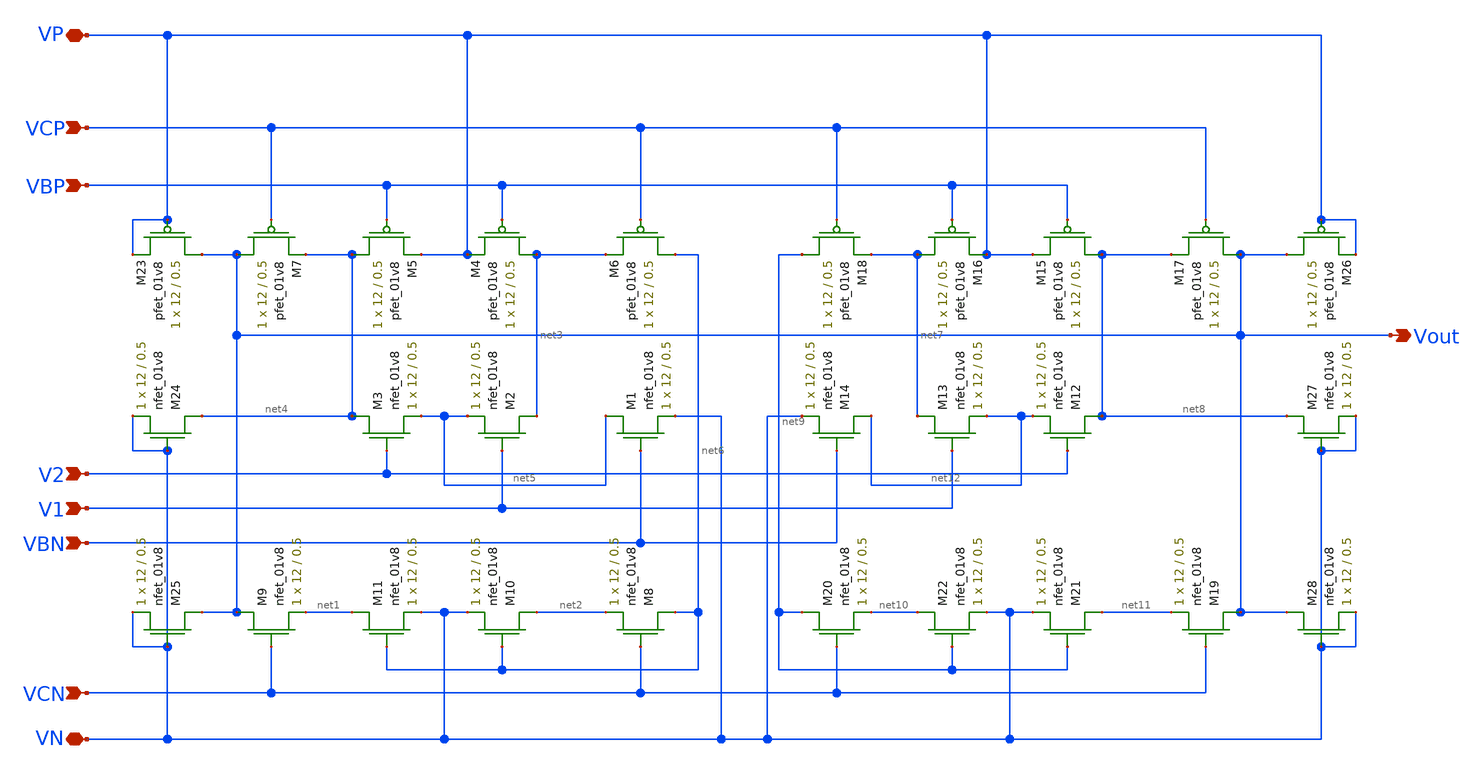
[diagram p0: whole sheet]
** sch_path: mp3/diff_amp/diff_amp_LDS_v3.sch
**.subckt diff_amp_LDS_v3 V1 V2 VN VBN VBP VP VCP VCN Vout
*.ipin V1
*.ipin V2
*.iopin VN
*.ipin VBN
*.ipin VBP
*.iopin VP
*.ipin VCP
*.ipin VCN
*.opin Vout
XM1 net5 VBN VN VN sky130_fd_pr__nfet_01v8 L=0.5 W=12 nf=1 ad='int((nf+1)/2) * W/nf * 0.29' as='int((nf+2)/2) * W/nf * 0.29'
+ pd='2*int((nf+1)/2) * (W/nf + 0.29)' ps='2*int((nf+2)/2) * (W/nf + 0.29)' nrd='0.29 / W' nrs='0.29 / W'
+ sa=0 sb=0 sd=0 mult=1 m=1
XM2 net3 V1 net5 VN sky130_fd_pr__nfet_01v8 L=0.5 W=12 nf=1 ad='int((nf+1)/2) * W/nf * 0.29' as='int((nf+2)/2) * W/nf * 0.29'
+ pd='2*int((nf+1)/2) * (W/nf + 0.29)' ps='2*int((nf+2)/2) * (W/nf + 0.29)' nrd='0.29 / W' nrs='0.29 / W'
+ sa=0 sb=0 sd=0 mult=1 m=1
XM3 net4 V2 net5 VN sky130_fd_pr__nfet_01v8 L=0.5 W=12 nf=1 ad='int((nf+1)/2) * W/nf * 0.29' as='int((nf+2)/2) * W/nf * 0.29'
+ pd='2*int((nf+1)/2) * (W/nf + 0.29)' ps='2*int((nf+2)/2) * (W/nf + 0.29)' nrd='0.29 / W' nrs='0.29 / W'
+ sa=0 sb=0 sd=0 mult=1 m=1
XM4 net3 VBP VP VP sky130_fd_pr__pfet_01v8 L=0.5 W=12 nf=1 ad='int((nf+1)/2) * W/nf * 0.29' as='int((nf+2)/2) * W/nf * 0.29'
+ pd='2*int((nf+1)/2) * (W/nf + 0.29)' ps='2*int((nf+2)/2) * (W/nf + 0.29)' nrd='0.29 / W' nrs='0.29 / W'
+ sa=0 sb=0 sd=0 mult=1 m=1
XM5 net4 VBP VP VP sky130_fd_pr__pfet_01v8 L=0.5 W=12 nf=1 ad='int((nf+1)/2) * W/nf * 0.29' as='int((nf+2)/2) * W/nf * 0.29'
+ pd='2*int((nf+1)/2) * (W/nf + 0.29)' ps='2*int((nf+2)/2) * (W/nf + 0.29)' nrd='0.29 / W' nrs='0.29 / W'
+ sa=0 sb=0 sd=0 mult=1 m=1
XM6 net6 VCP net3 VP sky130_fd_pr__pfet_01v8 L=0.5 W=12 nf=1 ad='int((nf+1)/2) * W/nf * 0.29' as='int((nf+2)/2) * W/nf * 0.29'
+ pd='2*int((nf+1)/2) * (W/nf + 0.29)' ps='2*int((nf+2)/2) * (W/nf + 0.29)' nrd='0.29 / W' nrs='0.29 / W'
+ sa=0 sb=0 sd=0 mult=1 m=1
XM7 Vout VCP net4 VP sky130_fd_pr__pfet_01v8 L=0.5 W=12 nf=1 ad='int((nf+1)/2) * W/nf * 0.29' as='int((nf+2)/2) * W/nf * 0.29'
+ pd='2*int((nf+1)/2) * (W/nf + 0.29)' ps='2*int((nf+2)/2) * (W/nf + 0.29)' nrd='0.29 / W' nrs='0.29 / W'
+ sa=0 sb=0 sd=0 mult=1 m=1
XM8 net6 VCN net2 VN sky130_fd_pr__nfet_01v8 L=0.5 W=12 nf=1 ad='int((nf+1)/2) * W/nf * 0.29' as='int((nf+2)/2) * W/nf * 0.29'
+ pd='2*int((nf+1)/2) * (W/nf + 0.29)' ps='2*int((nf+2)/2) * (W/nf + 0.29)' nrd='0.29 / W' nrs='0.29 / W'
+ sa=0 sb=0 sd=0 mult=1 m=1
XM9 Vout VCN net1 VN sky130_fd_pr__nfet_01v8 L=0.5 W=12 nf=1 ad='int((nf+1)/2) * W/nf * 0.29' as='int((nf+2)/2) * W/nf * 0.29'
+ pd='2*int((nf+1)/2) * (W/nf + 0.29)' ps='2*int((nf+2)/2) * (W/nf + 0.29)' nrd='0.29 / W' nrs='0.29 / W'
+ sa=0 sb=0 sd=0 mult=1 m=1
XM10 net2 net6 VN VN sky130_fd_pr__nfet_01v8 L=0.5 W=12 nf=1 ad='int((nf+1)/2) * W/nf * 0.29' as='int((nf+2)/2) * W/nf * 0.29'
+ pd='2*int((nf+1)/2) * (W/nf + 0.29)' ps='2*int((nf+2)/2) * (W/nf + 0.29)' nrd='0.29 / W' nrs='0.29 / W'
+ sa=0 sb=0 sd=0 mult=1 m=1
XM11 net1 net6 VN VN sky130_fd_pr__nfet_01v8 L=0.5 W=12 nf=1 ad='int((nf+1)/2) * W/nf * 0.29' as='int((nf+2)/2) * W/nf * 0.29'
+ pd='2*int((nf+1)/2) * (W/nf + 0.29)' ps='2*int((nf+2)/2) * (W/nf + 0.29)' nrd='0.29 / W' nrs='0.29 / W'
+ sa=0 sb=0 sd=0 mult=1 m=1
XM12 net8 V2 net12 VN sky130_fd_pr__nfet_01v8 L=0.5 W=12 nf=1 ad='int((nf+1)/2) * W/nf * 0.29' as='int((nf+2)/2) * W/nf * 0.29'
+ pd='2*int((nf+1)/2) * (W/nf + 0.29)' ps='2*int((nf+2)/2) * (W/nf + 0.29)' nrd='0.29 / W' nrs='0.29 / W'
+ sa=0 sb=0 sd=0 mult=1 m=1
XM13 net7 V1 net12 VN sky130_fd_pr__nfet_01v8 L=0.5 W=12 nf=1 ad='int((nf+1)/2) * W/nf * 0.29' as='int((nf+2)/2) * W/nf * 0.29'
+ pd='2*int((nf+1)/2) * (W/nf + 0.29)' ps='2*int((nf+2)/2) * (W/nf + 0.29)' nrd='0.29 / W' nrs='0.29 / W'
+ sa=0 sb=0 sd=0 mult=1 m=1
XM14 net12 VBN VN VN sky130_fd_pr__nfet_01v8 L=0.5 W=12 nf=1 ad='int((nf+1)/2) * W/nf * 0.29' as='int((nf+2)/2) * W/nf * 0.29'
+ pd='2*int((nf+1)/2) * (W/nf + 0.29)' ps='2*int((nf+2)/2) * (W/nf + 0.29)' nrd='0.29 / W' nrs='0.29 / W'
+ sa=0 sb=0 sd=0 mult=1 m=1
XM15 net8 VBP VP VP sky130_fd_pr__pfet_01v8 L=0.5 W=12 nf=1 ad='int((nf+1)/2) * W/nf * 0.29' as='int((nf+2)/2) * W/nf * 0.29'
+ pd='2*int((nf+1)/2) * (W/nf + 0.29)' ps='2*int((nf+2)/2) * (W/nf + 0.29)' nrd='0.29 / W' nrs='0.29 / W'
+ sa=0 sb=0 sd=0 mult=1 m=1
XM16 net7 VBP VP VP sky130_fd_pr__pfet_01v8 L=0.5 W=12 nf=1 ad='int((nf+1)/2) * W/nf * 0.29' as='int((nf+2)/2) * W/nf * 0.29'
+ pd='2*int((nf+1)/2) * (W/nf + 0.29)' ps='2*int((nf+2)/2) * (W/nf + 0.29)' nrd='0.29 / W' nrs='0.29 / W'
+ sa=0 sb=0 sd=0 mult=1 m=1
XM17 Vout VCP net8 VP sky130_fd_pr__pfet_01v8 L=0.5 W=12 nf=1 ad='int((nf+1)/2) * W/nf * 0.29' as='int((nf+2)/2) * W/nf * 0.29'
+ pd='2*int((nf+1)/2) * (W/nf + 0.29)' ps='2*int((nf+2)/2) * (W/nf + 0.29)' nrd='0.29 / W' nrs='0.29 / W'
+ sa=0 sb=0 sd=0 mult=1 m=1
XM18 net9 VCP net7 VP sky130_fd_pr__pfet_01v8 L=0.5 W=12 nf=1 ad='int((nf+1)/2) * W/nf * 0.29' as='int((nf+2)/2) * W/nf * 0.29'
+ pd='2*int((nf+1)/2) * (W/nf + 0.29)' ps='2*int((nf+2)/2) * (W/nf + 0.29)' nrd='0.29 / W' nrs='0.29 / W'
+ sa=0 sb=0 sd=0 mult=1 m=1
XM19 Vout VCN net11 VN sky130_fd_pr__nfet_01v8 L=0.5 W=12 nf=1 ad='int((nf+1)/2) * W/nf * 0.29' as='int((nf+2)/2) * W/nf * 0.29'
+ pd='2*int((nf+1)/2) * (W/nf + 0.29)' ps='2*int((nf+2)/2) * (W/nf + 0.29)' nrd='0.29 / W' nrs='0.29 / W'
+ sa=0 sb=0 sd=0 mult=1 m=1
XM20 net9 VCN net10 VN sky130_fd_pr__nfet_01v8 L=0.5 W=12 nf=1 ad='int((nf+1)/2) * W/nf * 0.29' as='int((nf+2)/2) * W/nf * 0.29'
+ pd='2*int((nf+1)/2) * (W/nf + 0.29)' ps='2*int((nf+2)/2) * (W/nf + 0.29)' nrd='0.29 / W' nrs='0.29 / W'
+ sa=0 sb=0 sd=0 mult=1 m=1
XM21 net11 net9 VN VN sky130_fd_pr__nfet_01v8 L=0.5 W=12 nf=1 ad='int((nf+1)/2) * W/nf * 0.29' as='int((nf+2)/2) * W/nf * 0.29'
+ pd='2*int((nf+1)/2) * (W/nf + 0.29)' ps='2*int((nf+2)/2) * (W/nf + 0.29)' nrd='0.29 / W' nrs='0.29 / W'
+ sa=0 sb=0 sd=0 mult=1 m=1
XM22 net10 net9 VN VN sky130_fd_pr__nfet_01v8 L=0.5 W=12 nf=1 ad='int((nf+1)/2) * W/nf * 0.29' as='int((nf+2)/2) * W/nf * 0.29'
+ pd='2*int((nf+1)/2) * (W/nf + 0.29)' ps='2*int((nf+2)/2) * (W/nf + 0.29)' nrd='0.29 / W' nrs='0.29 / W'
+ sa=0 sb=0 sd=0 mult=1 m=1
XM23 Vout VP VP VP sky130_fd_pr__pfet_01v8 L=0.5 W=12 nf=1 ad='int((nf+1)/2) * W/nf * 0.29' as='int((nf+2)/2) * W/nf * 0.29'
+ pd='2*int((nf+1)/2) * (W/nf + 0.29)' ps='2*int((nf+2)/2) * (W/nf + 0.29)' nrd='0.29 / W' nrs='0.29 / W'
+ sa=0 sb=0 sd=0 mult=1 m=1
XM24 net4 VN VN VN sky130_fd_pr__nfet_01v8 L=0.5 W=12 nf=1 ad='int((nf+1)/2) * W/nf * 0.29' as='int((nf+2)/2) * W/nf * 0.29'
+ pd='2*int((nf+1)/2) * (W/nf + 0.29)' ps='2*int((nf+2)/2) * (W/nf + 0.29)' nrd='0.29 / W' nrs='0.29 / W'
+ sa=0 sb=0 sd=0 mult=1 m=1
XM25 Vout VN VN VN sky130_fd_pr__nfet_01v8 L=0.5 W=12 nf=1 ad='int((nf+1)/2) * W/nf * 0.29' as='int((nf+2)/2) * W/nf * 0.29'
+ pd='2*int((nf+1)/2) * (W/nf + 0.29)' ps='2*int((nf+2)/2) * (W/nf + 0.29)' nrd='0.29 / W' nrs='0.29 / W'
+ sa=0 sb=0 sd=0 mult=1 m=1
XM26 Vout VP VP VP sky130_fd_pr__pfet_01v8 L=0.5 W=12 nf=1 ad='int((nf+1)/2) * W/nf * 0.29' as='int((nf+2)/2) * W/nf * 0.29'
+ pd='2*int((nf+1)/2) * (W/nf + 0.29)' ps='2*int((nf+2)/2) * (W/nf + 0.29)' nrd='0.29 / W' nrs='0.29 / W'
+ sa=0 sb=0 sd=0 mult=1 m=1
XM27 net8 VN VN VN sky130_fd_pr__nfet_01v8 L=0.5 W=12 nf=1 ad='int((nf+1)/2) * W/nf * 0.29' as='int((nf+2)/2) * W/nf * 0.29'
+ pd='2*int((nf+1)/2) * (W/nf + 0.29)' ps='2*int((nf+2)/2) * (W/nf + 0.29)' nrd='0.29 / W' nrs='0.29 / W'
+ sa=0 sb=0 sd=0 mult=1 m=1
XM28 Vout VN VN VN sky130_fd_pr__nfet_01v8 L=0.5 W=12 nf=1 ad='int((nf+1)/2) * W/nf * 0.29' as='int((nf+2)/2) * W/nf * 0.29'
+ pd='2*int((nf+1)/2) * (W/nf + 0.29)' ps='2*int((nf+2)/2) * (W/nf + 0.29)' nrd='0.29 / W' nrs='0.29 / W'
+ sa=0 sb=0 sd=0 mult=1 m=1
**.ends
.end
